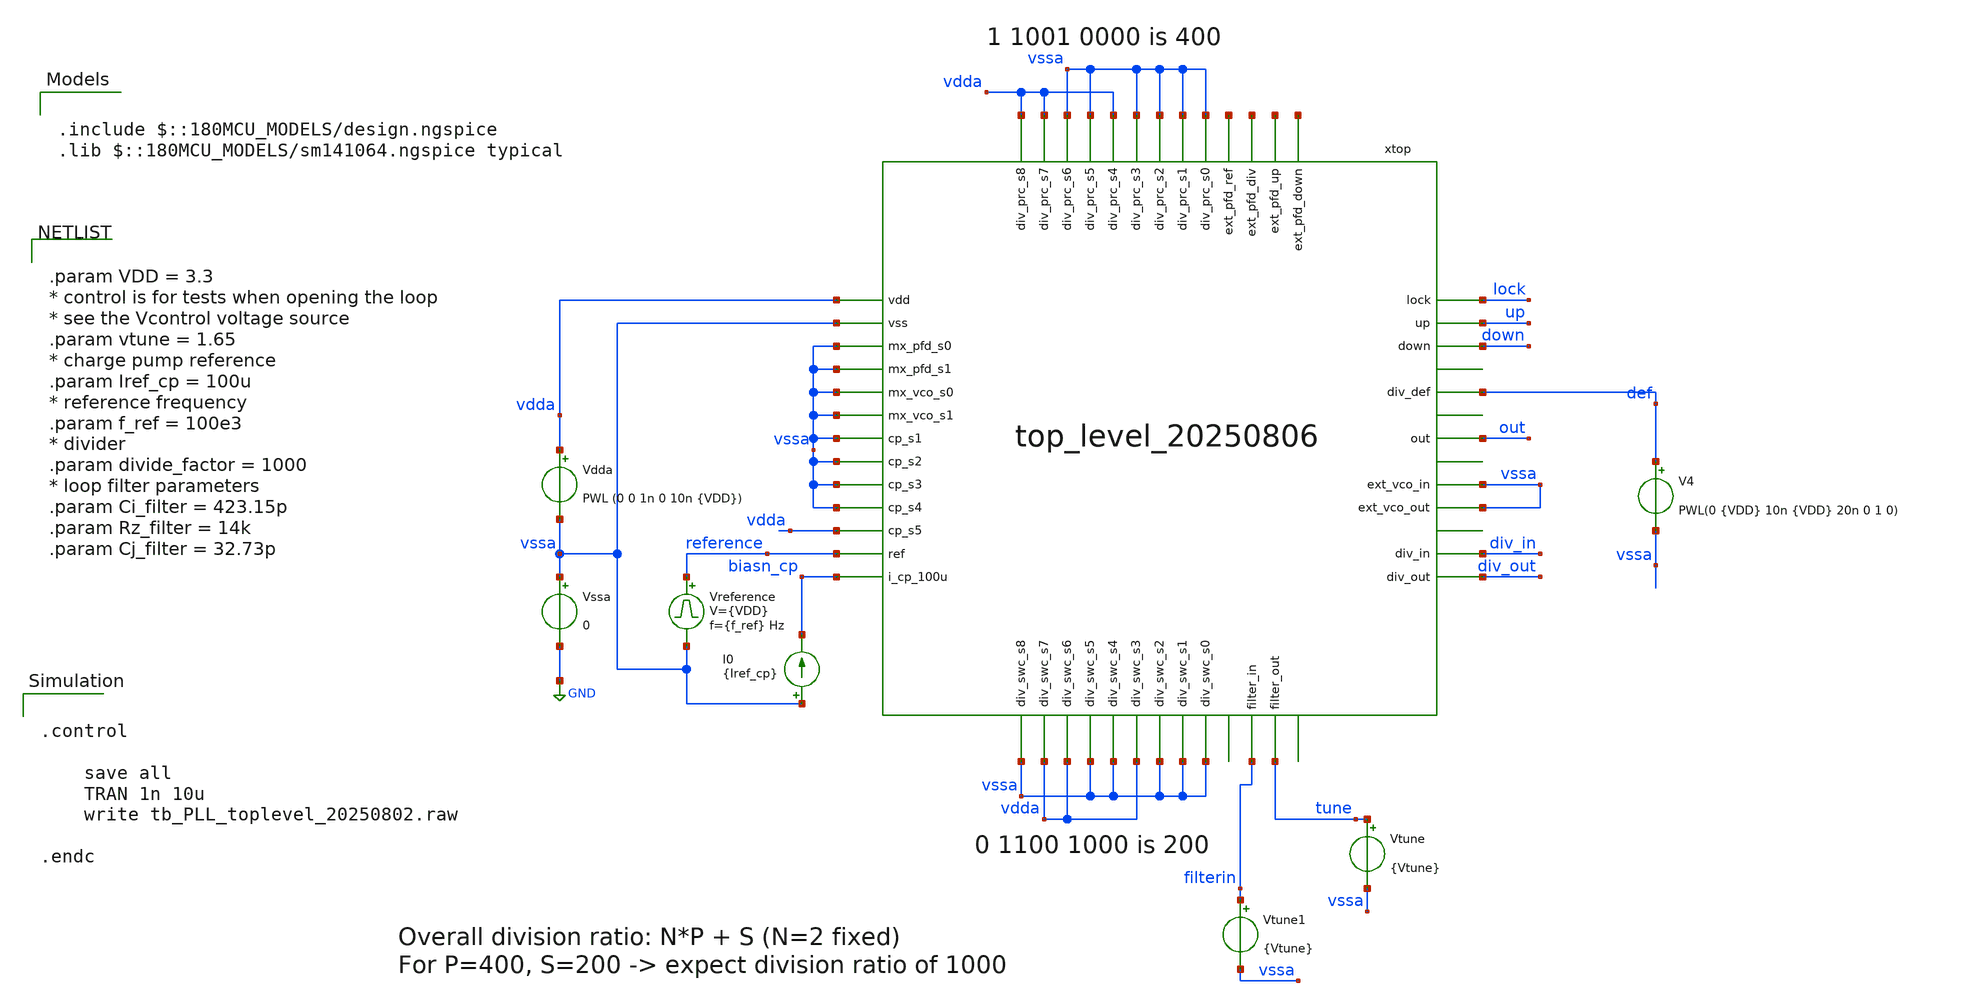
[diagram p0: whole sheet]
** sch_path: designs/libs/tb_top_level/tb_top_level_20250806.sch
**.subckt tb_top_level_20250806
Vreference reference vssa pulse 0 {VDD} '0.495/ {f_ref} ' '0.01/{f_ref} ' '0.01/{f_ref} ' '0.49/{f_ref} '
+ '1/{f_ref} '
Vssa vssa GND 0
Vdda vdda vssa PWL (0 0 1n 0 10n {VDD})
Vtune tune vssa {Vtune}
I0 vssa biasn_cp {Iref_cp}
V4 def vssa PWL(0 {VDD} 10n {VDD} 20n 0 1 0)
Vtune1 filterin vssa {Vtune}
xtop vdda vssa vssa vssa vssa vssa vssa vssa vssa vssa vssa vdda vdda vdda vssa vssa vdda vssa vssa
+ vssa vdda vdda vssa vssa vdda vssa vssa vssa vssa reference biasn_cp net1 net2 net3 net4 lock up down
+ tune vssa div_in div_out out filterin vssa def top_level_20250806
**** begin user architecture code


.control

    save all
    TRAN 1n 10u
    write tb_PLL_toplevel_20250802.raw

.endc




.param VDD = 3.3
* control is for tests when opening the loop
* see the Vcontrol voltage source
.param vtune = 1.65
* charge pump reference
.param Iref_cp = 100u
* reference frequency
.param f_ref = 100e3
* divider
.param divide_factor = 1000
* loop filter parameters
.param Ci_filter = 423.15p
.param Rz_filter = 14k
.param Cj_filter = 32.73p



.include $::180MCU_MODELS/design.ngspice
.lib $::180MCU_MODELS/sm141064.ngspice typical

**** end user architecture code
**.ends
.GLOBAL GND
.end
